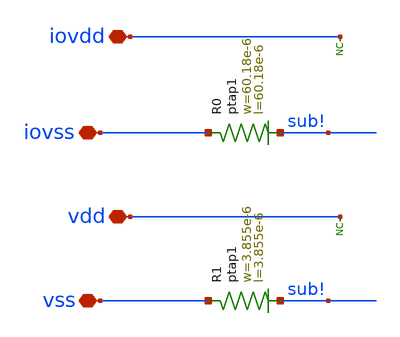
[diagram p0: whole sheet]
** sch_path: ihp-sg13g2/libs.ref/sg13g2_io/sch/xschem/sg13g2_Filler10000.sch
**.subckt sg13g2_Filler10000 iovdd iovss vdd vss
*.iopin iovdd
*.iopin iovss
*.iopin vdd
*.iopin vss
* noconn iovdd
* noconn vdd
XR0 iovss sub! ptap1 R=253.7m w=60.18e-6 l=60.18e-6
XR1 vss sub! ptap1 R=32.36 w=3.855e-6 l=3.855e-6
**.ends
.end
